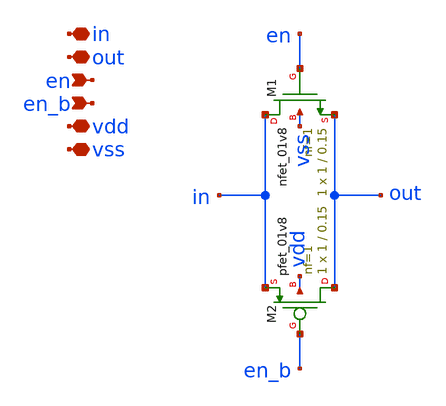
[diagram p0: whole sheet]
** sch_path: implementation/schematic/transmission_gate/transmission_gate.sch
**.subckt transmission_gate in out en en_b vdd vss
*.iopin in
*.iopin out
*.ipin en
*.ipin en_b
*.iopin vdd
*.iopin vss
XM1 in en out vss sky130_fd_pr__nfet_01v8 L=0.15 W=1 nf=1 ad='int((nf+1)/2) * W/nf * 0.29' as='int((nf+2)/2) * W/nf * 0.29'
+ pd='2*int((nf+1)/2) * (W/nf + 0.29)' ps='2*int((nf+2)/2) * (W/nf + 0.29)' nrd='0.29 / W' nrs='0.29 / W'
+ sa=0 sb=0 sd=0 mult=1 m=1
XM2 out en_b in vdd sky130_fd_pr__pfet_01v8 L=0.15 W=1 nf=1 ad='int((nf+1)/2) * W/nf * 0.29' as='int((nf+2)/2) * W/nf * 0.29'
+ pd='2*int((nf+1)/2) * (W/nf + 0.29)' ps='2*int((nf+2)/2) * (W/nf + 0.29)' nrd='0.29 / W' nrs='0.29 / W'
+ sa=0 sb=0 sd=0 mult=1 m=1
**.ends
.end
